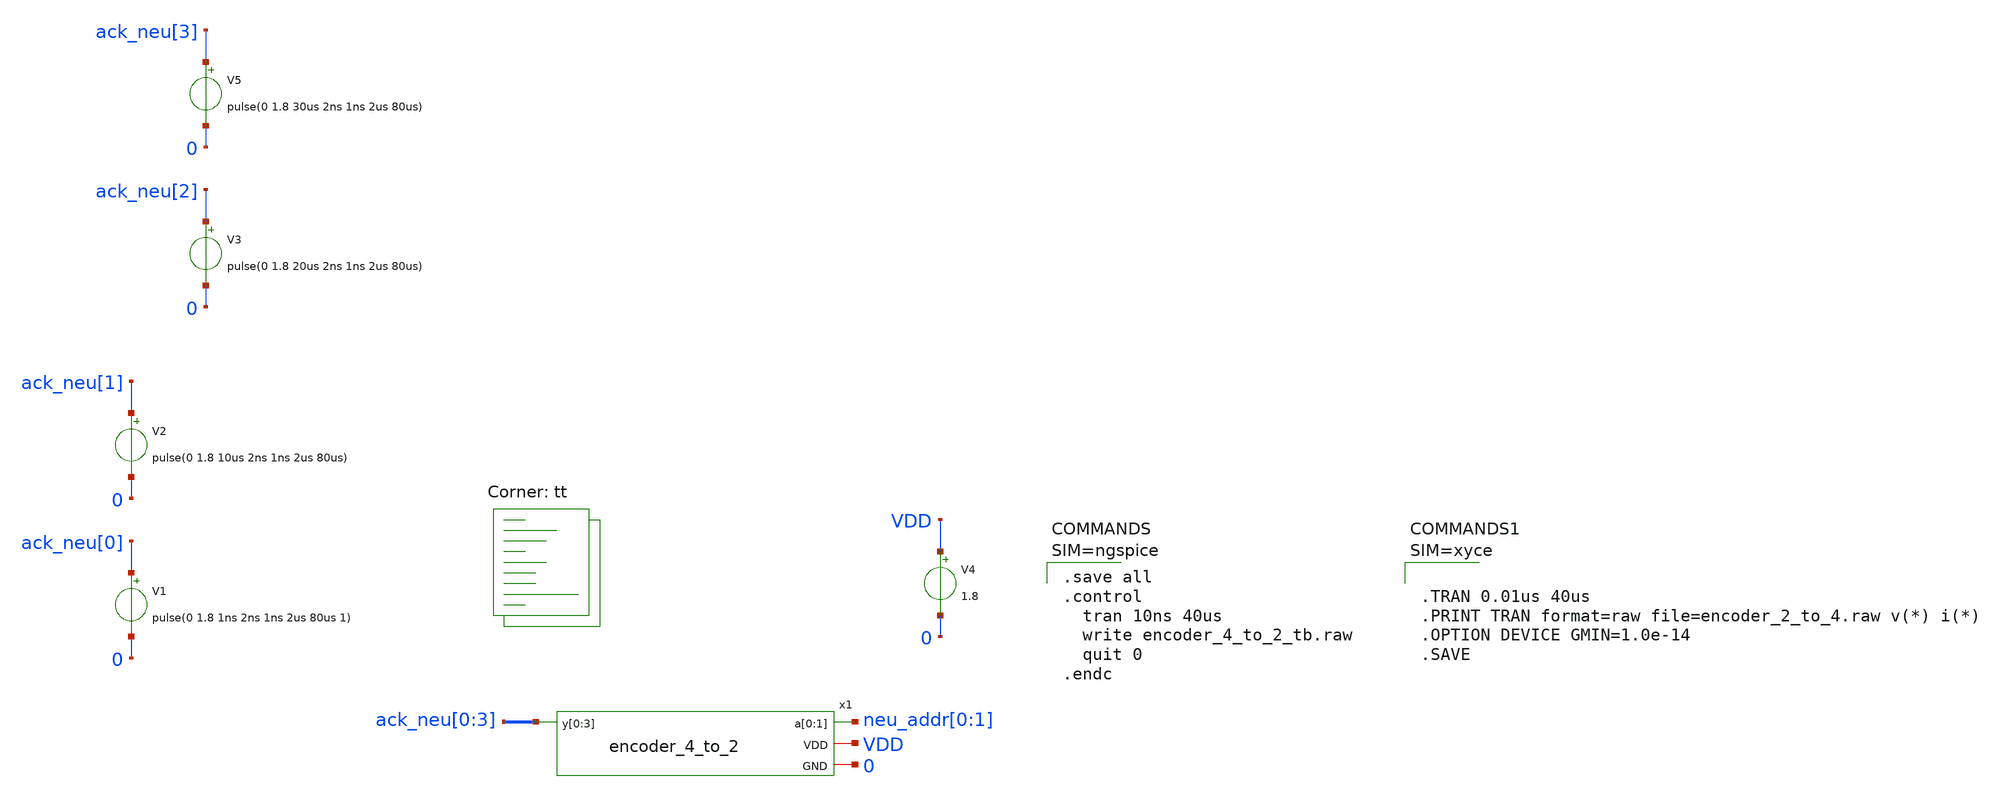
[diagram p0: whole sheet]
** sch_path: design/xschem/encoder_4_to_2_tb.sch
**.subckt encoder_4_to_2_tb
V1 ack_neu[0] 0 pulse(0 1.8 1ns 2ns 1ns 2us 80us 1)
V2 ack_neu[1] 0 pulse(0 1.8 10us 2ns 1ns 2us 80us)
V4 VDD 0 1.8
x1 ack_neu[0] ack_neu[1] ack_neu[2] ack_neu[3] neu_addr[0] neu_addr[1] VDD 0 encoder_4_to_2
V3 ack_neu[2] 0 pulse(0 1.8 20us 2ns 1ns 2us 80us)
V5 ack_neu[3] 0 pulse(0 1.8 30us 2ns 1ns 2us 80us)
**** begin user architecture code


* Standard cell simulation files
.include $::SKYWATER_STDCELLS/sky130_fd_sc_hd.spice


.lib $::SKYWATER_MODELS/sky130.lib.spice tt


.save all
.control
  tran 10ns 40us
  write encoder_4_to_2_tb.raw
  quit 0
.endc






**** end user architecture code
**.ends

* expanding   symbol:  encoder_4_to_2.sym # of pins=4
** sym_path: design/xschem/encoder_4_to_2.sym
** sch_path: design/xschem/encoder_4_to_2.sch
.subckt encoder_4_to_2 y[0] y[1] y[2] y[3] a[0] a[1] VDD GND
*.opin a[0],a[1]
*.ipin y[0],y[1],y[2],y[3]
*.iopin VDD
*.iopin GND
x1 y[3] y[2] GND GND VDD VDD a[1] sky130_fd_sc_hd__or2_0
x2 y[3] y[1] GND GND VDD VDD a[0] sky130_fd_sc_hd__or2_0
.ends

.end
